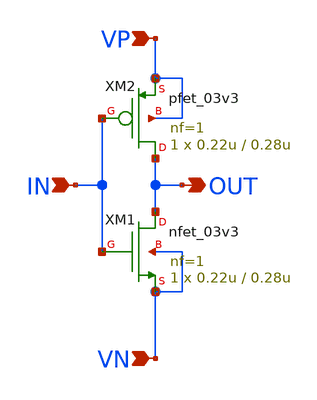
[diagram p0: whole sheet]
** sch_path: designs/libs/Inverter/inverter.sch
**.subckt inverter IN OUT VP VN
*.ipin IN
*.opin OUT
*.ipin VP
*.ipin VN
XM1 OUT IN VN VN nfet_03v3 L=0.28u W=0.22u nf=1 ad='int((nf+1)/2) * W/nf * 0.18u' as='int((nf+2)/2) * W/nf * 0.18u'
+ pd='2*int((nf+1)/2) * (W/nf + 0.18u)' ps='2*int((nf+2)/2) * (W/nf + 0.18u)' nrd='0.18u / W' nrs='0.18u / W'
+ sa=0 sb=0 sd=0 m=1
XM2 OUT IN VP VP pfet_03v3 L=0.28u W=0.22u nf=1 ad='int((nf+1)/2) * W/nf * 0.18u' as='int((nf+2)/2) * W/nf * 0.18u'
+ pd='2*int((nf+1)/2) * (W/nf + 0.18u)' ps='2*int((nf+2)/2) * (W/nf + 0.18u)' nrd='0.18u / W' nrs='0.18u / W'
+ sa=0 sb=0 sd=0 m=1
**.ends
.end
